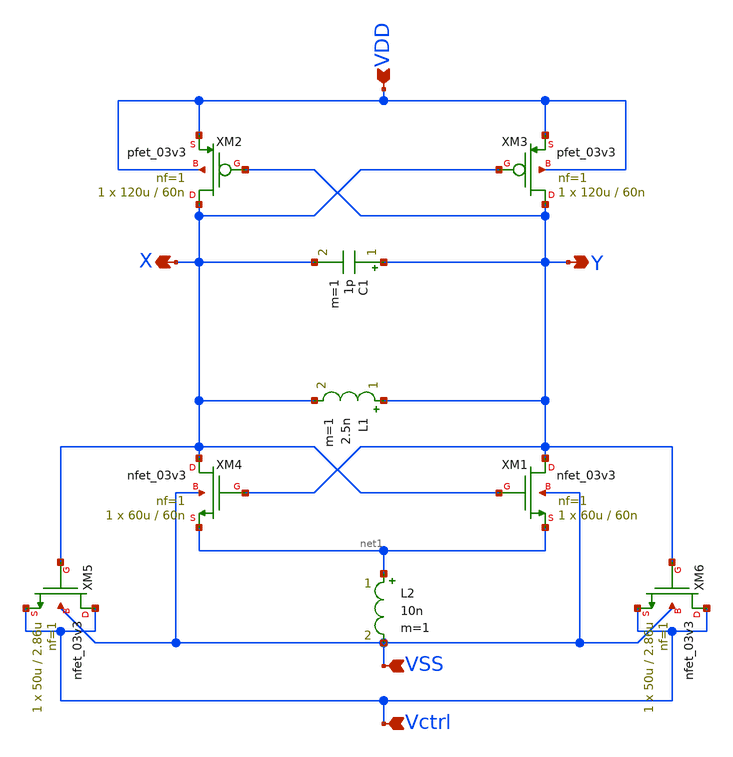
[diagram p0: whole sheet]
** sch_path: Project/1-on-chip/schematic/VCO/lcvco.sch
**.subckt lcvco VDD Vctrl X Y VSS
*.ipin VDD
*.ipin Vctrl
*.opin X
*.opin Y
*.ipin VSS
XM1 Y X net1 VSS nfet_03v3 L=60n W=60u nf=1 ad='int((nf+1)/2) * W/nf * 0.18u' as='int((nf+2)/2) * W/nf * 0.18u'
+ pd='2*int((nf+1)/2) * (W/nf + 0.18u)' ps='2*int((nf+2)/2) * (W/nf + 0.18u)' nrd='0.18u / W' nrs='0.18u / W'
+ sa=0 sb=0 sd=0 m=1
XM2 X Y VDD VDD pfet_03v3 L=60n W=120u nf=1 ad='int((nf+1)/2) * W/nf * 0.18u' as='int((nf+2)/2) * W/nf * 0.18u'
+ pd='2*int((nf+1)/2) * (W/nf + 0.18u)' ps='2*int((nf+2)/2) * (W/nf + 0.18u)' nrd='0.18u / W' nrs='0.18u / W'
+ sa=0 sb=0 sd=0 m=1
XM3 Y X VDD VDD pfet_03v3 L=60n W=120u nf=1 ad='int((nf+1)/2) * W/nf * 0.18u' as='int((nf+2)/2) * W/nf * 0.18u'
+ pd='2*int((nf+1)/2) * (W/nf + 0.18u)' ps='2*int((nf+2)/2) * (W/nf + 0.18u)' nrd='0.18u / W' nrs='0.18u / W'
+ sa=0 sb=0 sd=0 m=1
XM4 X Y net1 VSS nfet_03v3 L=60n W=60u nf=1 ad='int((nf+1)/2) * W/nf * 0.18u' as='int((nf+2)/2) * W/nf * 0.18u'
+ pd='2*int((nf+1)/2) * (W/nf + 0.18u)' ps='2*int((nf+2)/2) * (W/nf + 0.18u)' nrd='0.18u / W' nrs='0.18u / W'
+ sa=0 sb=0 sd=0 m=1
XM5 Vctrl X Vctrl VSS nfet_03v3 L=2.86u W=50u nf=1 ad='int((nf+1)/2) * W/nf * 0.18u' as='int((nf+2)/2) * W/nf * 0.18u'
+ pd='2*int((nf+1)/2) * (W/nf + 0.18u)' ps='2*int((nf+2)/2) * (W/nf + 0.18u)' nrd='0.18u / W' nrs='0.18u / W'
+ sa=0 sb=0 sd=0 m=1
XM6 Vctrl Y Vctrl VSS nfet_03v3 L=2.86u W=50u nf=1 ad='int((nf+1)/2) * W/nf * 0.18u' as='int((nf+2)/2) * W/nf * 0.18u'
+ pd='2*int((nf+1)/2) * (W/nf + 0.18u)' ps='2*int((nf+2)/2) * (W/nf + 0.18u)' nrd='0.18u / W' nrs='0.18u / W'
+ sa=0 sb=0 sd=0 m=1
L1 Y X 2.5n m=1
L2 net1 VSS 10n m=1
C1 Y X 1p m=1
**.ends
.end
